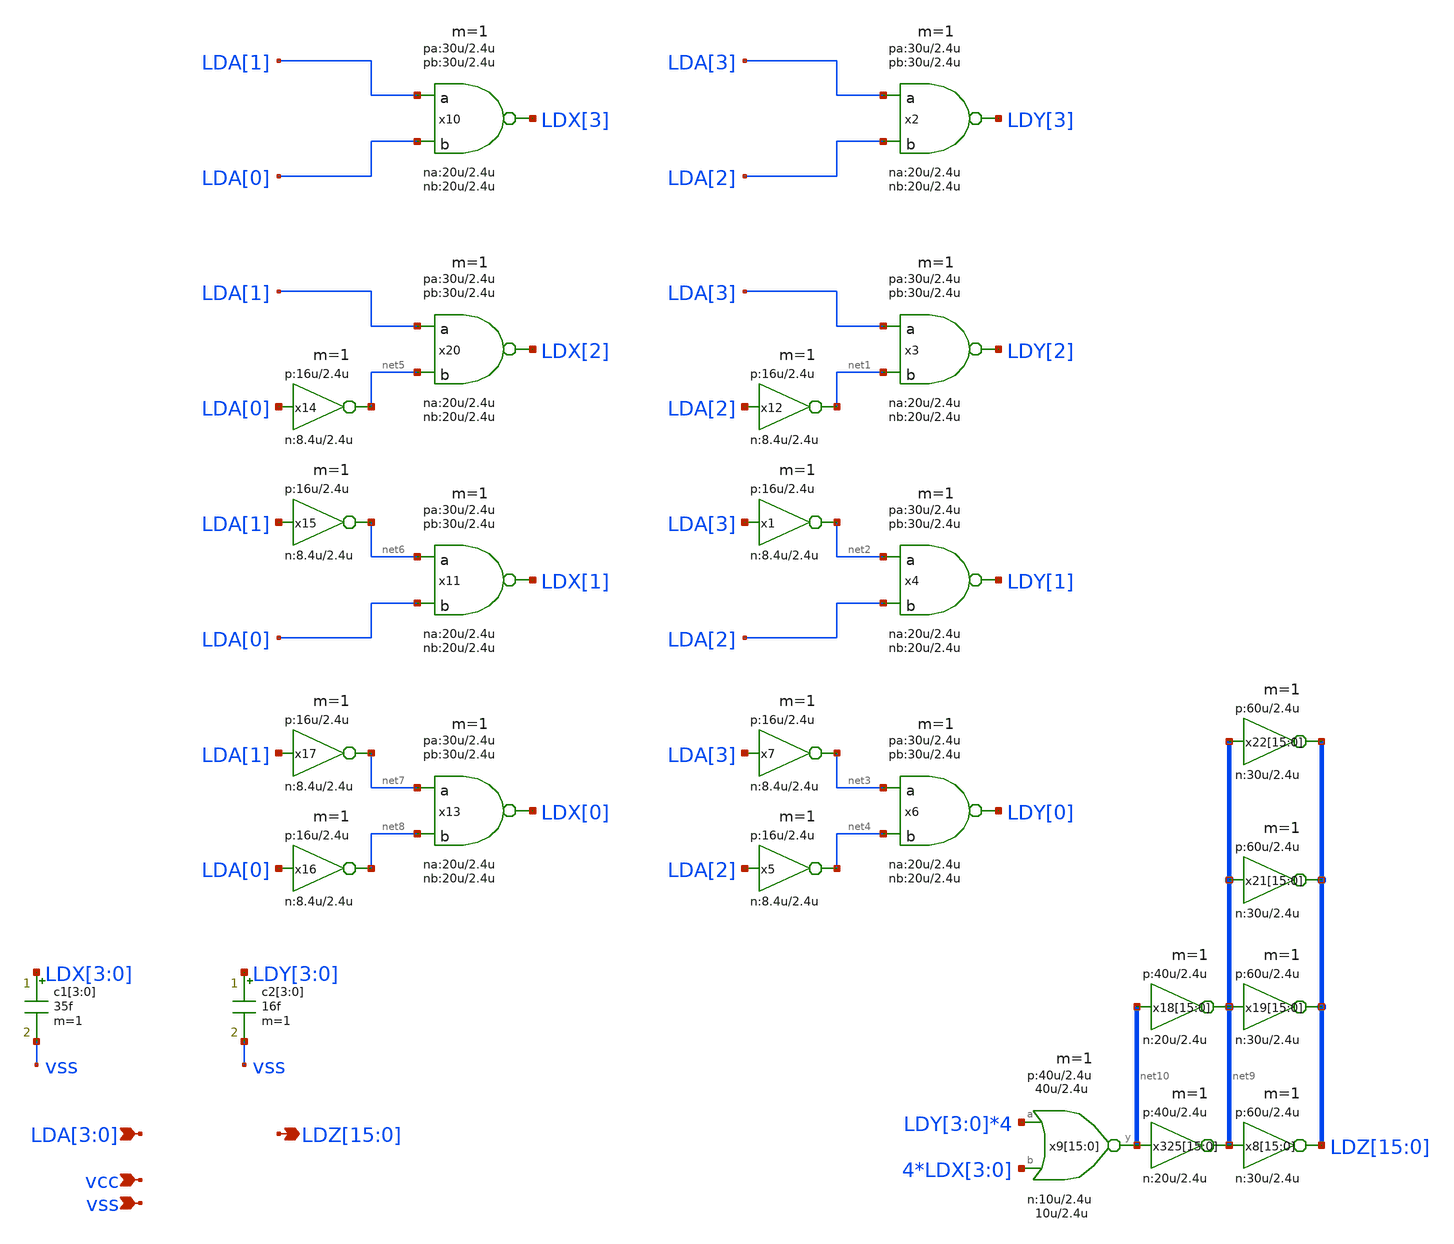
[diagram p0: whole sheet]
** sch_path: xschem_library/rom8k/rom2_predec1.sch
**.subckt rom2_predec1
*+ LDZ[15],LDZ[14],LDZ[13],LDZ[12],LDZ[11],LDZ[10],LDZ[9],LDZ[8],LDZ[7],LDZ[6],LDZ[5],LDZ[4],LDZ[3],LDZ[2],LDZ[1],LDZ[0] LDA[3],LDA[2],LDA[1],LDA[0] vcc vss
*.opin
*+ LDZ[15],LDZ[14],LDZ[13],LDZ[12],LDZ[11],LDZ[10],LDZ[9],LDZ[8],LDZ[7],LDZ[6],LDZ[5],LDZ[4],LDZ[3],LDZ[2],LDZ[1],LDZ[0]
*.ipin LDA[3],LDA[2],LDA[1],LDA[0]
*.ipin vcc
*.ipin vss
x325[15] net9[15] net10[15] vcc vss lvnot wn=20u lln=2.4u wp=40u lp=2.4u m=1
x325[14] net9[14] net10[14] vcc vss lvnot wn=20u lln=2.4u wp=40u lp=2.4u m=1
x325[13] net9[13] net10[13] vcc vss lvnot wn=20u lln=2.4u wp=40u lp=2.4u m=1
x325[12] net9[12] net10[12] vcc vss lvnot wn=20u lln=2.4u wp=40u lp=2.4u m=1
x325[11] net9[11] net10[11] vcc vss lvnot wn=20u lln=2.4u wp=40u lp=2.4u m=1
x325[10] net9[10] net10[10] vcc vss lvnot wn=20u lln=2.4u wp=40u lp=2.4u m=1
x325[9] net9[9] net10[9] vcc vss lvnot wn=20u lln=2.4u wp=40u lp=2.4u m=1
x325[8] net9[8] net10[8] vcc vss lvnot wn=20u lln=2.4u wp=40u lp=2.4u m=1
x325[7] net9[7] net10[7] vcc vss lvnot wn=20u lln=2.4u wp=40u lp=2.4u m=1
x325[6] net9[6] net10[6] vcc vss lvnot wn=20u lln=2.4u wp=40u lp=2.4u m=1
x325[5] net9[5] net10[5] vcc vss lvnot wn=20u lln=2.4u wp=40u lp=2.4u m=1
x325[4] net9[4] net10[4] vcc vss lvnot wn=20u lln=2.4u wp=40u lp=2.4u m=1
x325[3] net9[3] net10[3] vcc vss lvnot wn=20u lln=2.4u wp=40u lp=2.4u m=1
x325[2] net9[2] net10[2] vcc vss lvnot wn=20u lln=2.4u wp=40u lp=2.4u m=1
x325[1] net9[1] net10[1] vcc vss lvnot wn=20u lln=2.4u wp=40u lp=2.4u m=1
x325[0] net9[0] net10[0] vcc vss lvnot wn=20u lln=2.4u wp=40u lp=2.4u m=1
x8[15] LDZ[15] net9[15] vcc vss lvnot wn=30u lln=2.4u wp=60u lp=2.4u m=1
x8[14] LDZ[14] net9[14] vcc vss lvnot wn=30u lln=2.4u wp=60u lp=2.4u m=1
x8[13] LDZ[13] net9[13] vcc vss lvnot wn=30u lln=2.4u wp=60u lp=2.4u m=1
x8[12] LDZ[12] net9[12] vcc vss lvnot wn=30u lln=2.4u wp=60u lp=2.4u m=1
x8[11] LDZ[11] net9[11] vcc vss lvnot wn=30u lln=2.4u wp=60u lp=2.4u m=1
x8[10] LDZ[10] net9[10] vcc vss lvnot wn=30u lln=2.4u wp=60u lp=2.4u m=1
x8[9] LDZ[9] net9[9] vcc vss lvnot wn=30u lln=2.4u wp=60u lp=2.4u m=1
x8[8] LDZ[8] net9[8] vcc vss lvnot wn=30u lln=2.4u wp=60u lp=2.4u m=1
x8[7] LDZ[7] net9[7] vcc vss lvnot wn=30u lln=2.4u wp=60u lp=2.4u m=1
x8[6] LDZ[6] net9[6] vcc vss lvnot wn=30u lln=2.4u wp=60u lp=2.4u m=1
x8[5] LDZ[5] net9[5] vcc vss lvnot wn=30u lln=2.4u wp=60u lp=2.4u m=1
x8[4] LDZ[4] net9[4] vcc vss lvnot wn=30u lln=2.4u wp=60u lp=2.4u m=1
x8[3] LDZ[3] net9[3] vcc vss lvnot wn=30u lln=2.4u wp=60u lp=2.4u m=1
x8[2] LDZ[2] net9[2] vcc vss lvnot wn=30u lln=2.4u wp=60u lp=2.4u m=1
x8[1] LDZ[1] net9[1] vcc vss lvnot wn=30u lln=2.4u wp=60u lp=2.4u m=1
x8[0] LDZ[0] net9[0] vcc vss lvnot wn=30u lln=2.4u wp=60u lp=2.4u m=1
x9[15] net10[15] LDY[3] LDX[3] vcc vss lvnor2 wna=10u lna=2.4u wpa=40u lpa=2.4u wnb=10u lnb=2.4u
+ wpb=40u lpb=2.4u m=1
x9[14] net10[14] LDY[3] LDX[2] vcc vss lvnor2 wna=10u lna=2.4u wpa=40u lpa=2.4u wnb=10u lnb=2.4u
+ wpb=40u lpb=2.4u m=1
x9[13] net10[13] LDY[3] LDX[1] vcc vss lvnor2 wna=10u lna=2.4u wpa=40u lpa=2.4u wnb=10u lnb=2.4u
+ wpb=40u lpb=2.4u m=1
x9[12] net10[12] LDY[3] LDX[0] vcc vss lvnor2 wna=10u lna=2.4u wpa=40u lpa=2.4u wnb=10u lnb=2.4u
+ wpb=40u lpb=2.4u m=1
x9[11] net10[11] LDY[2] LDX[3] vcc vss lvnor2 wna=10u lna=2.4u wpa=40u lpa=2.4u wnb=10u lnb=2.4u
+ wpb=40u lpb=2.4u m=1
x9[10] net10[10] LDY[2] LDX[2] vcc vss lvnor2 wna=10u lna=2.4u wpa=40u lpa=2.4u wnb=10u lnb=2.4u
+ wpb=40u lpb=2.4u m=1
x9[9] net10[9] LDY[2] LDX[1] vcc vss lvnor2 wna=10u lna=2.4u wpa=40u lpa=2.4u wnb=10u lnb=2.4u
+ wpb=40u lpb=2.4u m=1
x9[8] net10[8] LDY[2] LDX[0] vcc vss lvnor2 wna=10u lna=2.4u wpa=40u lpa=2.4u wnb=10u lnb=2.4u
+ wpb=40u lpb=2.4u m=1
x9[7] net10[7] LDY[1] LDX[3] vcc vss lvnor2 wna=10u lna=2.4u wpa=40u lpa=2.4u wnb=10u lnb=2.4u
+ wpb=40u lpb=2.4u m=1
x9[6] net10[6] LDY[1] LDX[2] vcc vss lvnor2 wna=10u lna=2.4u wpa=40u lpa=2.4u wnb=10u lnb=2.4u
+ wpb=40u lpb=2.4u m=1
x9[5] net10[5] LDY[1] LDX[1] vcc vss lvnor2 wna=10u lna=2.4u wpa=40u lpa=2.4u wnb=10u lnb=2.4u
+ wpb=40u lpb=2.4u m=1
x9[4] net10[4] LDY[1] LDX[0] vcc vss lvnor2 wna=10u lna=2.4u wpa=40u lpa=2.4u wnb=10u lnb=2.4u
+ wpb=40u lpb=2.4u m=1
x9[3] net10[3] LDY[0] LDX[3] vcc vss lvnor2 wna=10u lna=2.4u wpa=40u lpa=2.4u wnb=10u lnb=2.4u
+ wpb=40u lpb=2.4u m=1
x9[2] net10[2] LDY[0] LDX[2] vcc vss lvnor2 wna=10u lna=2.4u wpa=40u lpa=2.4u wnb=10u lnb=2.4u
+ wpb=40u lpb=2.4u m=1
x9[1] net10[1] LDY[0] LDX[1] vcc vss lvnor2 wna=10u lna=2.4u wpa=40u lpa=2.4u wnb=10u lnb=2.4u
+ wpb=40u lpb=2.4u m=1
x9[0] net10[0] LDY[0] LDX[0] vcc vss lvnor2 wna=10u lna=2.4u wpa=40u lpa=2.4u wnb=10u lnb=2.4u
+ wpb=40u lpb=2.4u m=1
c1[3] LDX[3] vss 35f m=1
c1[2] LDX[2] vss 35f m=1
c1[1] LDX[1] vss 35f m=1
c1[0] LDX[0] vss 35f m=1
c2[3] LDY[3] vss 16f m=1
c2[2] LDY[2] vss 16f m=1
c2[1] LDY[1] vss 16f m=1
c2[0] LDY[0] vss 16f m=1
x2 LDY[3] LDA[3] LDA[2] vcc vss lvnand2 wna=20u lna=2.4u wpa=30u lpa=2.4u wnb=20u lnb=2.4u wpb=30u
+ lpb=2.4u m=1
x3 LDY[2] LDA[3] net1 vcc vss lvnand2 wna=20u lna=2.4u wpa=30u lpa=2.4u wnb=20u lnb=2.4u wpb=30u
+ lpb=2.4u m=1
x4 LDY[1] net2 LDA[2] vcc vss lvnand2 wna=20u lna=2.4u wpa=30u lpa=2.4u wnb=20u lnb=2.4u wpb=30u
+ lpb=2.4u m=1
x6 LDY[0] net3 net4 vcc vss lvnand2 wna=20u lna=2.4u wpa=30u lpa=2.4u wnb=20u lnb=2.4u wpb=30u
+ lpb=2.4u m=1
x12 net1 LDA[2] vcc vss lvnot wn=8.4u lln=2.4u wp=16u lp=2.4u m=1
x1 net2 LDA[3] vcc vss lvnot wn=8.4u lln=2.4u wp=16u lp=2.4u m=1
x5 net4 LDA[2] vcc vss lvnot wn=8.4u lln=2.4u wp=16u lp=2.4u m=1
x7 net3 LDA[3] vcc vss lvnot wn=8.4u lln=2.4u wp=16u lp=2.4u m=1
x10 LDX[3] LDA[1] LDA[0] vcc vss lvnand2 wna=20u lna=2.4u wpa=30u lpa=2.4u wnb=20u lnb=2.4u wpb=30u
+ lpb=2.4u m=1
x20 LDX[2] LDA[1] net5 vcc vss lvnand2 wna=20u lna=2.4u wpa=30u lpa=2.4u wnb=20u lnb=2.4u wpb=30u
+ lpb=2.4u m=1
x11 LDX[1] net6 LDA[0] vcc vss lvnand2 wna=20u lna=2.4u wpa=30u lpa=2.4u wnb=20u lnb=2.4u wpb=30u
+ lpb=2.4u m=1
x13 LDX[0] net7 net8 vcc vss lvnand2 wna=20u lna=2.4u wpa=30u lpa=2.4u wnb=20u lnb=2.4u wpb=30u
+ lpb=2.4u m=1
x14 net5 LDA[0] vcc vss lvnot wn=8.4u lln=2.4u wp=16u lp=2.4u m=1
x15 net6 LDA[1] vcc vss lvnot wn=8.4u lln=2.4u wp=16u lp=2.4u m=1
x16 net8 LDA[0] vcc vss lvnot wn=8.4u lln=2.4u wp=16u lp=2.4u m=1
x17 net7 LDA[1] vcc vss lvnot wn=8.4u lln=2.4u wp=16u lp=2.4u m=1
x18[15] net9[15] net10[15] vcc vss lvnot wn=20u lln=2.4u wp=40u lp=2.4u m=1
x18[14] net9[14] net10[14] vcc vss lvnot wn=20u lln=2.4u wp=40u lp=2.4u m=1
x18[13] net9[13] net10[13] vcc vss lvnot wn=20u lln=2.4u wp=40u lp=2.4u m=1
x18[12] net9[12] net10[12] vcc vss lvnot wn=20u lln=2.4u wp=40u lp=2.4u m=1
x18[11] net9[11] net10[11] vcc vss lvnot wn=20u lln=2.4u wp=40u lp=2.4u m=1
x18[10] net9[10] net10[10] vcc vss lvnot wn=20u lln=2.4u wp=40u lp=2.4u m=1
x18[9] net9[9] net10[9] vcc vss lvnot wn=20u lln=2.4u wp=40u lp=2.4u m=1
x18[8] net9[8] net10[8] vcc vss lvnot wn=20u lln=2.4u wp=40u lp=2.4u m=1
x18[7] net9[7] net10[7] vcc vss lvnot wn=20u lln=2.4u wp=40u lp=2.4u m=1
x18[6] net9[6] net10[6] vcc vss lvnot wn=20u lln=2.4u wp=40u lp=2.4u m=1
x18[5] net9[5] net10[5] vcc vss lvnot wn=20u lln=2.4u wp=40u lp=2.4u m=1
x18[4] net9[4] net10[4] vcc vss lvnot wn=20u lln=2.4u wp=40u lp=2.4u m=1
x18[3] net9[3] net10[3] vcc vss lvnot wn=20u lln=2.4u wp=40u lp=2.4u m=1
x18[2] net9[2] net10[2] vcc vss lvnot wn=20u lln=2.4u wp=40u lp=2.4u m=1
x18[1] net9[1] net10[1] vcc vss lvnot wn=20u lln=2.4u wp=40u lp=2.4u m=1
x18[0] net9[0] net10[0] vcc vss lvnot wn=20u lln=2.4u wp=40u lp=2.4u m=1
x19[15] LDZ[15] net9[15] vcc vss lvnot wn=30u lln=2.4u wp=60u lp=2.4u m=1
x19[14] LDZ[14] net9[14] vcc vss lvnot wn=30u lln=2.4u wp=60u lp=2.4u m=1
x19[13] LDZ[13] net9[13] vcc vss lvnot wn=30u lln=2.4u wp=60u lp=2.4u m=1
x19[12] LDZ[12] net9[12] vcc vss lvnot wn=30u lln=2.4u wp=60u lp=2.4u m=1
x19[11] LDZ[11] net9[11] vcc vss lvnot wn=30u lln=2.4u wp=60u lp=2.4u m=1
x19[10] LDZ[10] net9[10] vcc vss lvnot wn=30u lln=2.4u wp=60u lp=2.4u m=1
x19[9] LDZ[9] net9[9] vcc vss lvnot wn=30u lln=2.4u wp=60u lp=2.4u m=1
x19[8] LDZ[8] net9[8] vcc vss lvnot wn=30u lln=2.4u wp=60u lp=2.4u m=1
x19[7] LDZ[7] net9[7] vcc vss lvnot wn=30u lln=2.4u wp=60u lp=2.4u m=1
x19[6] LDZ[6] net9[6] vcc vss lvnot wn=30u lln=2.4u wp=60u lp=2.4u m=1
x19[5] LDZ[5] net9[5] vcc vss lvnot wn=30u lln=2.4u wp=60u lp=2.4u m=1
x19[4] LDZ[4] net9[4] vcc vss lvnot wn=30u lln=2.4u wp=60u lp=2.4u m=1
x19[3] LDZ[3] net9[3] vcc vss lvnot wn=30u lln=2.4u wp=60u lp=2.4u m=1
x19[2] LDZ[2] net9[2] vcc vss lvnot wn=30u lln=2.4u wp=60u lp=2.4u m=1
x19[1] LDZ[1] net9[1] vcc vss lvnot wn=30u lln=2.4u wp=60u lp=2.4u m=1
x19[0] LDZ[0] net9[0] vcc vss lvnot wn=30u lln=2.4u wp=60u lp=2.4u m=1
x21[15] LDZ[15] net9[15] vcc vss lvnot wn=30u lln=2.4u wp=60u lp=2.4u m=1
x21[14] LDZ[14] net9[14] vcc vss lvnot wn=30u lln=2.4u wp=60u lp=2.4u m=1
x21[13] LDZ[13] net9[13] vcc vss lvnot wn=30u lln=2.4u wp=60u lp=2.4u m=1
x21[12] LDZ[12] net9[12] vcc vss lvnot wn=30u lln=2.4u wp=60u lp=2.4u m=1
x21[11] LDZ[11] net9[11] vcc vss lvnot wn=30u lln=2.4u wp=60u lp=2.4u m=1
x21[10] LDZ[10] net9[10] vcc vss lvnot wn=30u lln=2.4u wp=60u lp=2.4u m=1
x21[9] LDZ[9] net9[9] vcc vss lvnot wn=30u lln=2.4u wp=60u lp=2.4u m=1
x21[8] LDZ[8] net9[8] vcc vss lvnot wn=30u lln=2.4u wp=60u lp=2.4u m=1
x21[7] LDZ[7] net9[7] vcc vss lvnot wn=30u lln=2.4u wp=60u lp=2.4u m=1
x21[6] LDZ[6] net9[6] vcc vss lvnot wn=30u lln=2.4u wp=60u lp=2.4u m=1
x21[5] LDZ[5] net9[5] vcc vss lvnot wn=30u lln=2.4u wp=60u lp=2.4u m=1
x21[4] LDZ[4] net9[4] vcc vss lvnot wn=30u lln=2.4u wp=60u lp=2.4u m=1
x21[3] LDZ[3] net9[3] vcc vss lvnot wn=30u lln=2.4u wp=60u lp=2.4u m=1
x21[2] LDZ[2] net9[2] vcc vss lvnot wn=30u lln=2.4u wp=60u lp=2.4u m=1
x21[1] LDZ[1] net9[1] vcc vss lvnot wn=30u lln=2.4u wp=60u lp=2.4u m=1
x21[0] LDZ[0] net9[0] vcc vss lvnot wn=30u lln=2.4u wp=60u lp=2.4u m=1
x22[15] LDZ[15] net9[15] vcc vss lvnot wn=30u lln=2.4u wp=60u lp=2.4u m=1
x22[14] LDZ[14] net9[14] vcc vss lvnot wn=30u lln=2.4u wp=60u lp=2.4u m=1
x22[13] LDZ[13] net9[13] vcc vss lvnot wn=30u lln=2.4u wp=60u lp=2.4u m=1
x22[12] LDZ[12] net9[12] vcc vss lvnot wn=30u lln=2.4u wp=60u lp=2.4u m=1
x22[11] LDZ[11] net9[11] vcc vss lvnot wn=30u lln=2.4u wp=60u lp=2.4u m=1
x22[10] LDZ[10] net9[10] vcc vss lvnot wn=30u lln=2.4u wp=60u lp=2.4u m=1
x22[9] LDZ[9] net9[9] vcc vss lvnot wn=30u lln=2.4u wp=60u lp=2.4u m=1
x22[8] LDZ[8] net9[8] vcc vss lvnot wn=30u lln=2.4u wp=60u lp=2.4u m=1
x22[7] LDZ[7] net9[7] vcc vss lvnot wn=30u lln=2.4u wp=60u lp=2.4u m=1
x22[6] LDZ[6] net9[6] vcc vss lvnot wn=30u lln=2.4u wp=60u lp=2.4u m=1
x22[5] LDZ[5] net9[5] vcc vss lvnot wn=30u lln=2.4u wp=60u lp=2.4u m=1
x22[4] LDZ[4] net9[4] vcc vss lvnot wn=30u lln=2.4u wp=60u lp=2.4u m=1
x22[3] LDZ[3] net9[3] vcc vss lvnot wn=30u lln=2.4u wp=60u lp=2.4u m=1
x22[2] LDZ[2] net9[2] vcc vss lvnot wn=30u lln=2.4u wp=60u lp=2.4u m=1
x22[1] LDZ[1] net9[1] vcc vss lvnot wn=30u lln=2.4u wp=60u lp=2.4u m=1
x22[0] LDZ[0] net9[0] vcc vss lvnot wn=30u lln=2.4u wp=60u lp=2.4u m=1
**.ends
.end
